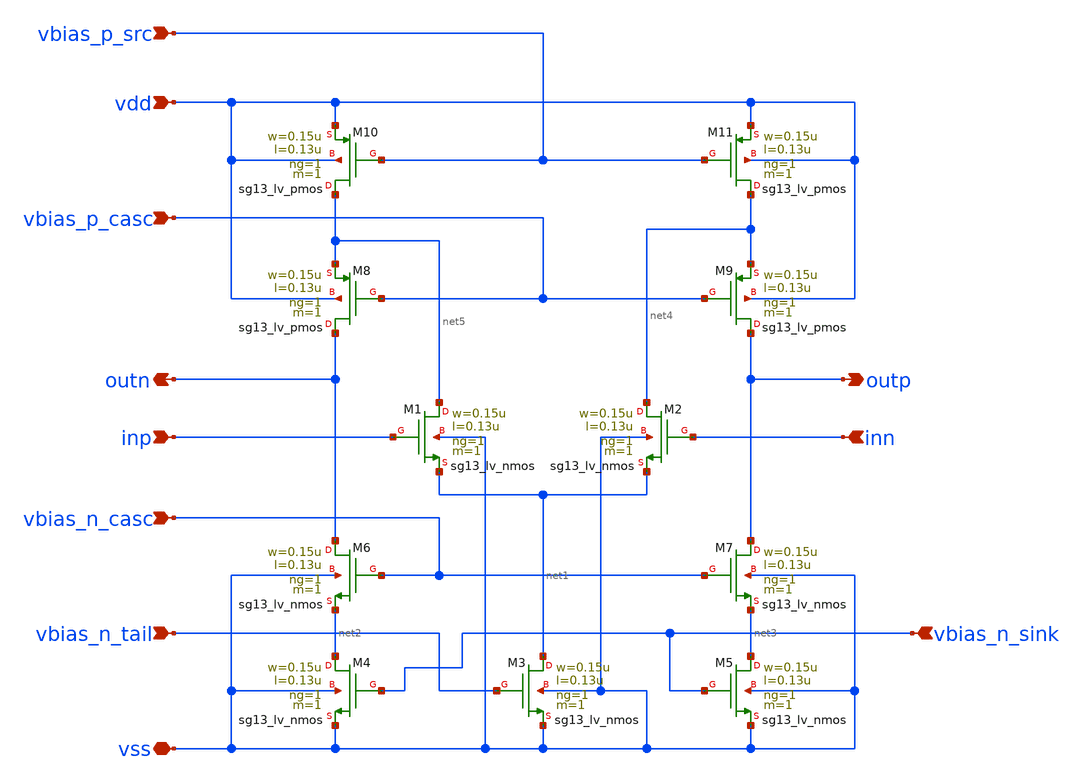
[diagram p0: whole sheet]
** sch_path: 3_real_circuits/ota_folded_cascoded.sch
**.subckt ota_folded_cascoded inp inn vss vdd outn outp vbias_n_casc vbias_p_casc vbias_p_src
*+ vbias_n_sink vbias_n_tail
*.ipin inp
*.ipin inn
*.iopin vss
*.ipin vdd
*.opin outn
*.opin outp
*.ipin vbias_n_casc
*.ipin vbias_p_casc
*.ipin vbias_p_src
*.ipin vbias_n_sink
*.ipin vbias_n_tail
XM1 net5 inp net1 vss sg13_lv_nmos w=0.15u l=0.13u ng=1 m=1 mm_ok=1
XM2 net4 inn net1 vss sg13_lv_nmos w=0.15u l=0.13u ng=1 m=1 mm_ok=1
XM3 net1 vbias_n_tail vss vss sg13_lv_nmos w=0.15u l=0.13u ng=1 m=1 mm_ok=1
XM6 outn vbias_n_casc net2 vss sg13_lv_nmos w=0.15u l=0.13u ng=1 m=1 mm_ok=1
XM4 net2 vbias_n_sink vss vss sg13_lv_nmos w=0.15u l=0.13u ng=1 m=1 mm_ok=1
XM7 outp vbias_n_casc net3 vss sg13_lv_nmos w=0.15u l=0.13u ng=1 m=1 mm_ok=1
XM5 net3 vbias_n_sink vss vss sg13_lv_nmos w=0.15u l=0.13u ng=1 m=1 mm_ok=1
XM9 outp vbias_p_casc net4 vdd sg13_lv_pmos w=0.15u l=0.13u ng=1 m=1 mm_ok=1
XM8 outn vbias_p_casc net5 vdd sg13_lv_pmos w=0.15u l=0.13u ng=1 m=1 mm_ok=1
XM10 net5 vbias_p_src vdd vdd sg13_lv_pmos w=0.15u l=0.13u ng=1 m=1 mm_ok=1
XM11 net4 vbias_p_src vdd vdd sg13_lv_pmos w=0.15u l=0.13u ng=1 m=1 mm_ok=1
**.ends
.end
